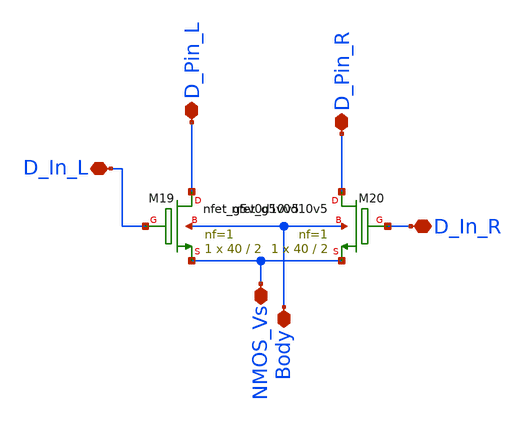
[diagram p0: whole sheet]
** sch_path: xschem/PrimalStructures/DifferentialPair.sch
**.subckt DifferentialPair D_Pin_L D_Pin_R D_In_L D_In_R NMOS_Vs Body
*.iopin D_Pin_L
*.iopin D_Pin_R
*.iopin D_In_L
*.iopin D_In_R
*.iopin NMOS_Vs
*.iopin Body
XM19 D_Pin_L D_In_L NMOS_Vs Body sky130_fd_pr__nfet_g5v0d10v5 L=2 W=40 nf=1 ad='int((nf+1)/2) * W/nf * 0.29'
+ as='int((nf+2)/2) * W/nf * 0.29' pd='2*int((nf+1)/2) * (W/nf + 0.29)' ps='2*int((nf+2)/2) * (W/nf + 0.29)'
+ nrd='0.29 / W' nrs='0.29 / W' sa=0 sb=0 sd=0 mult=1 m=1
XM20 D_Pin_R D_In_R NMOS_Vs Body sky130_fd_pr__nfet_g5v0d10v5 L=2 W=40 nf=1 ad='int((nf+1)/2) * W/nf * 0.29'
+ as='int((nf+2)/2) * W/nf * 0.29' pd='2*int((nf+1)/2) * (W/nf + 0.29)' ps='2*int((nf+2)/2) * (W/nf + 0.29)'
+ nrd='0.29 / W' nrs='0.29 / W' sa=0 sb=0 sd=0 mult=1 m=1
**.ends
.end
